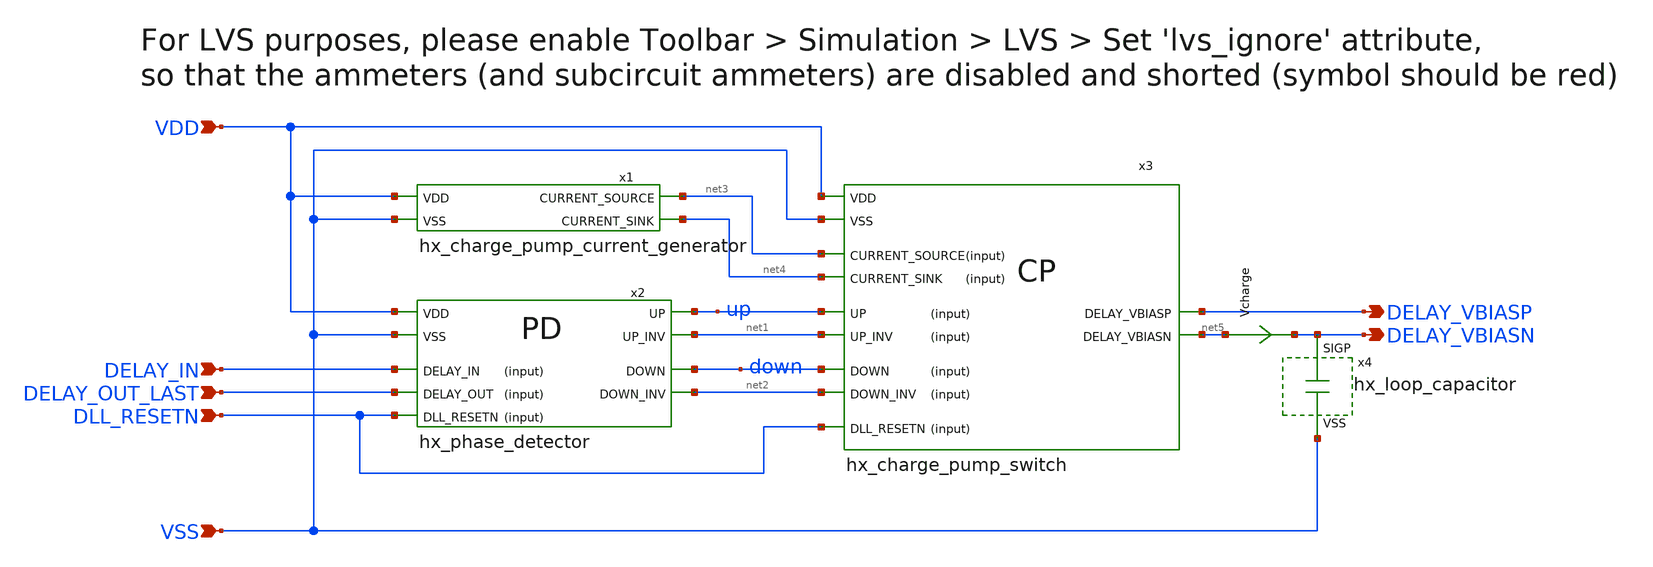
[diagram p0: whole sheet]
** sch_path: schematics/hx_dll_controller.sch
**.subckt hx_dll_controller VDD VSS DELAY_VBIASP DELAY_VBIASN DLL_RESETN DELAY_IN DELAY_OUT_LAST
*.ipin VDD
*.ipin VSS
*.opin DELAY_VBIASP
*.opin DELAY_VBIASN
*.ipin DLL_RESETN
*.ipin DELAY_IN
*.ipin DELAY_OUT_LAST
Vcharge net5 DELAY_VBIASN 0
.save i(vcharge)
x1 net4 VDD net3 VSS hx_charge_pump_current_generator
x2 VSS VDD net1 down net2 DLL_RESETN DELAY_IN up DELAY_OUT_LAST hx_phase_detector
x4 DELAY_VBIASN VSS hx_loop_capacitor
x3 VSS VDD net1 down net2 up DELAY_VBIASP net5 net3 net4 DLL_RESETN hx_charge_pump_switch
**.ends
.end
